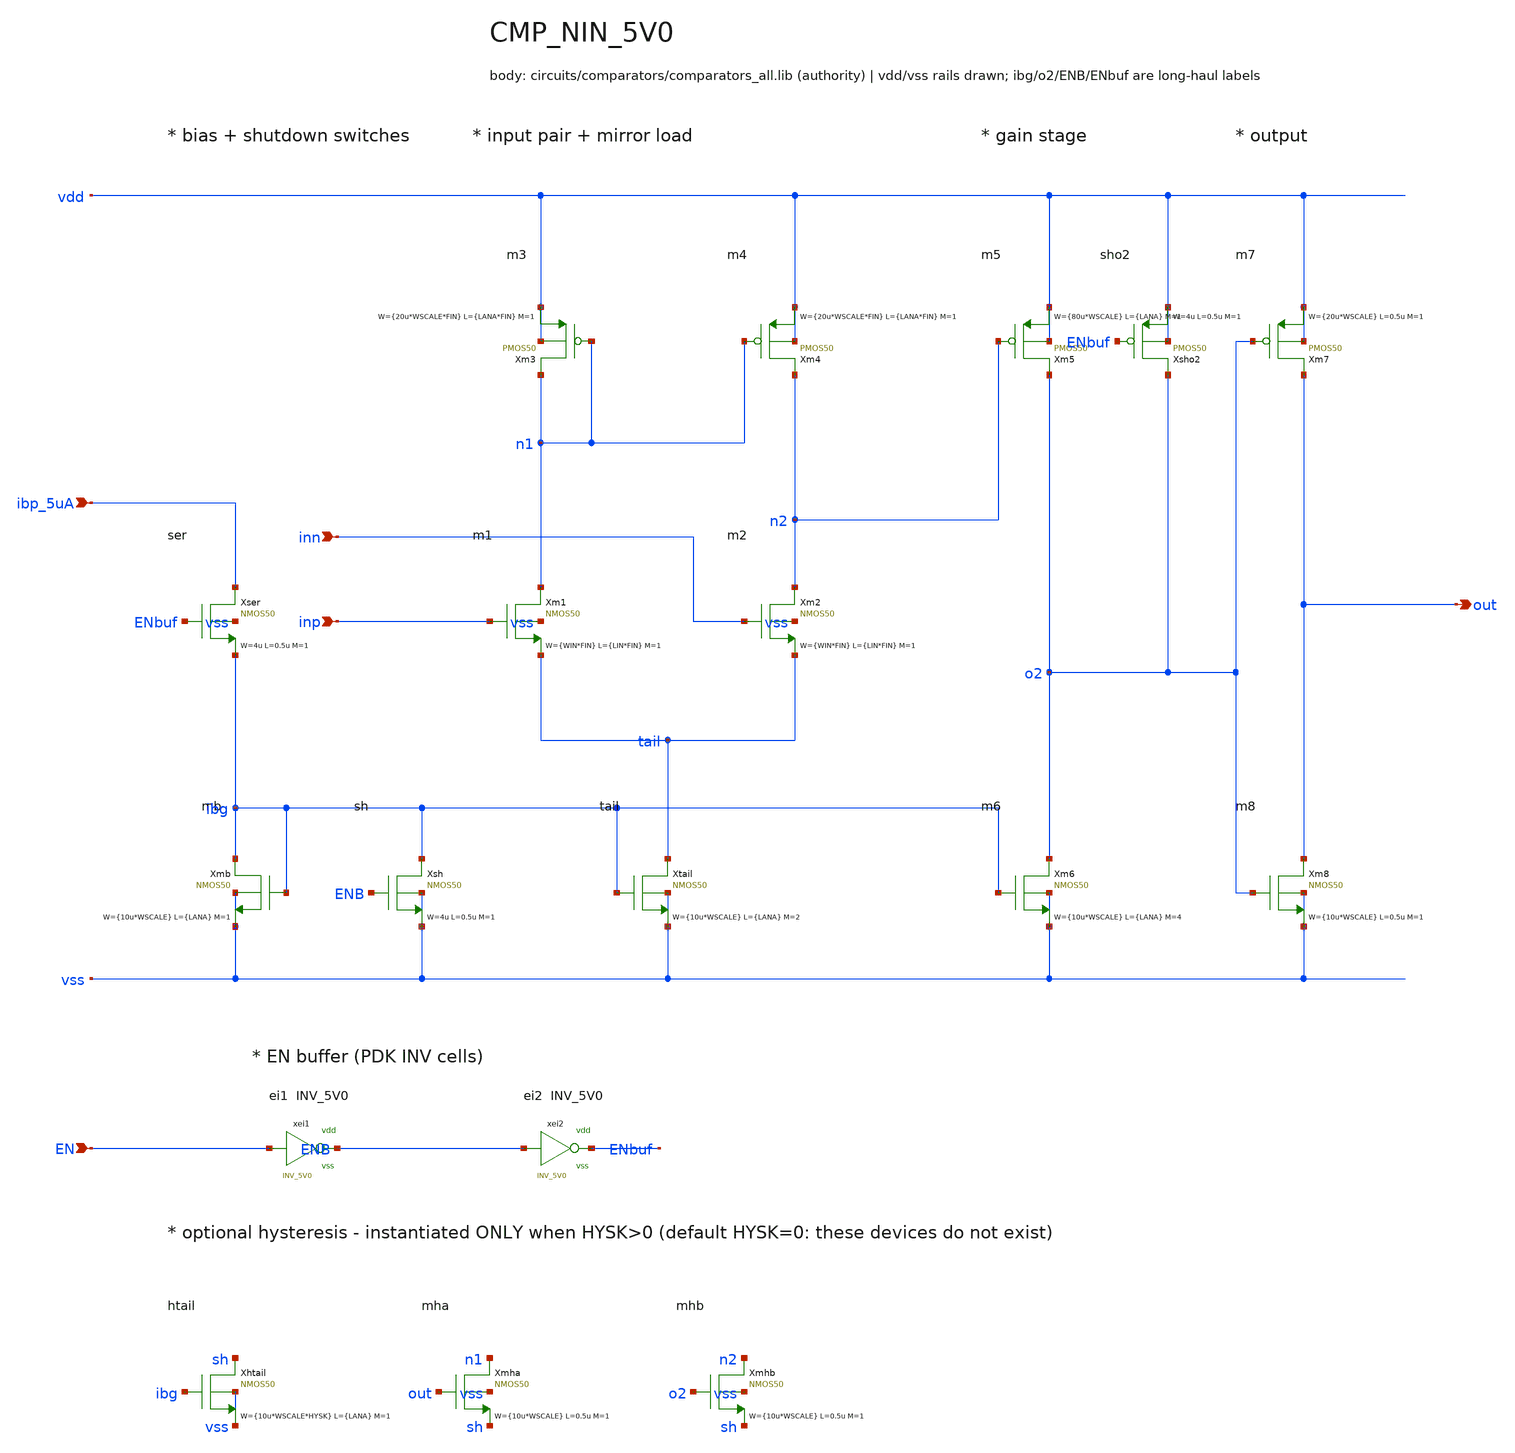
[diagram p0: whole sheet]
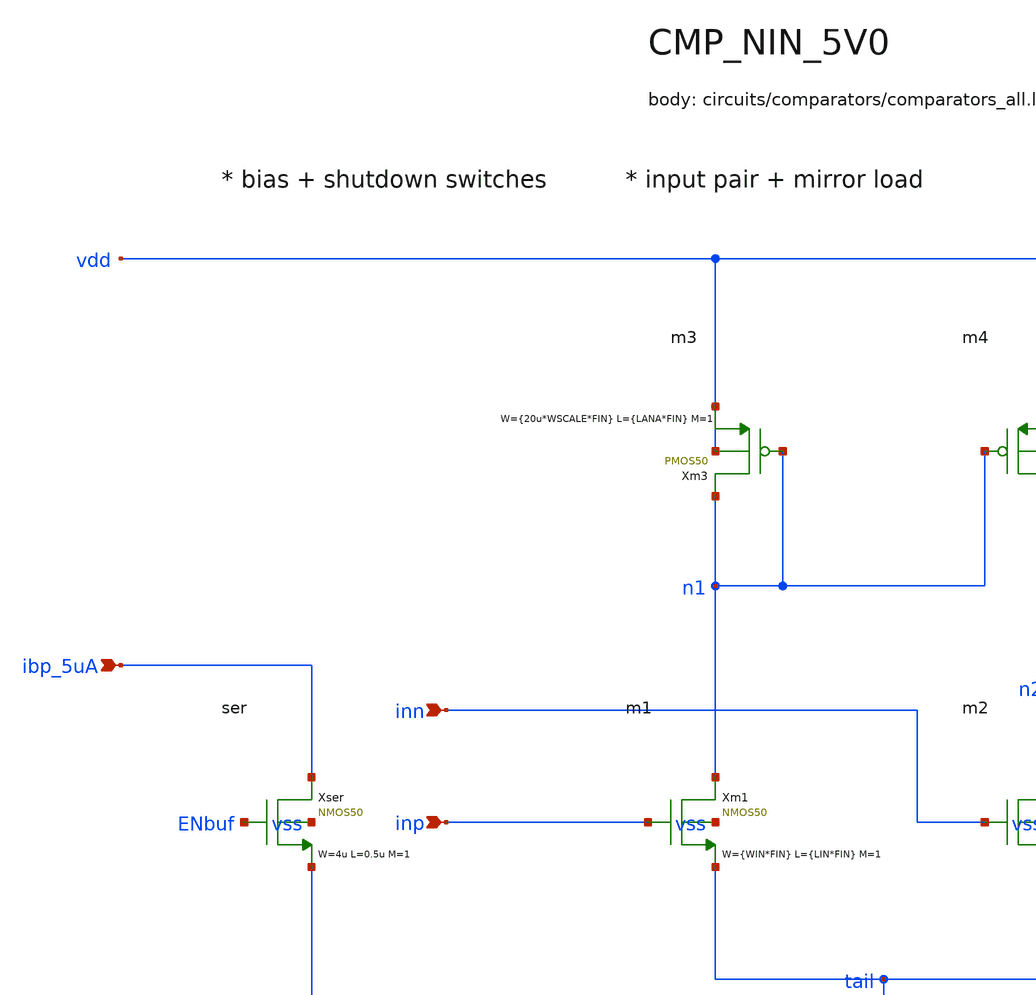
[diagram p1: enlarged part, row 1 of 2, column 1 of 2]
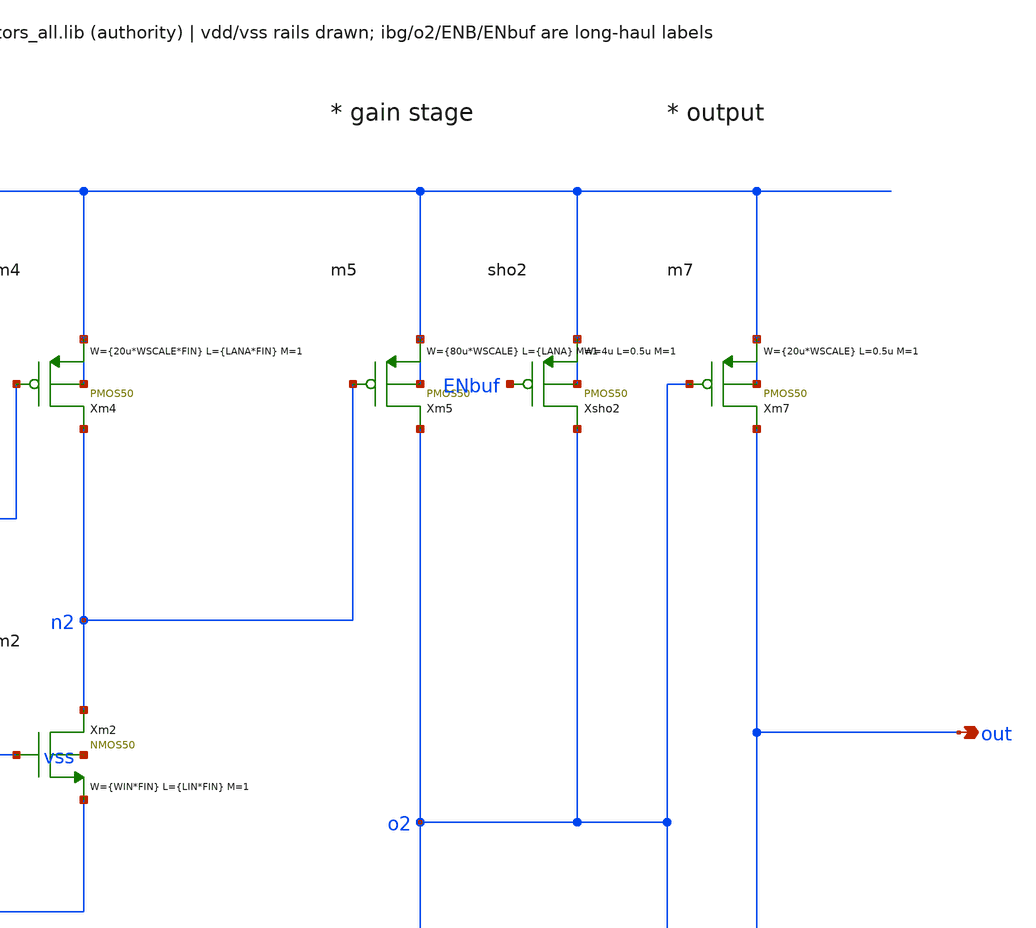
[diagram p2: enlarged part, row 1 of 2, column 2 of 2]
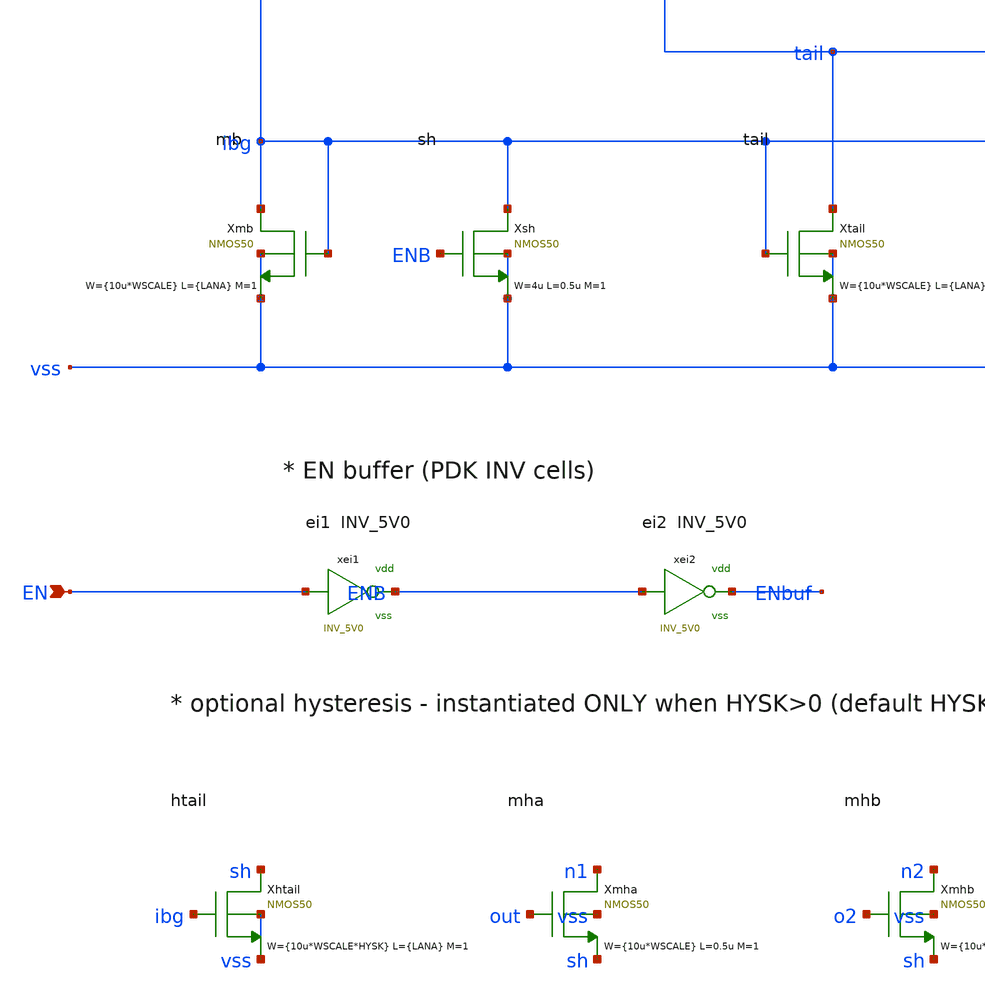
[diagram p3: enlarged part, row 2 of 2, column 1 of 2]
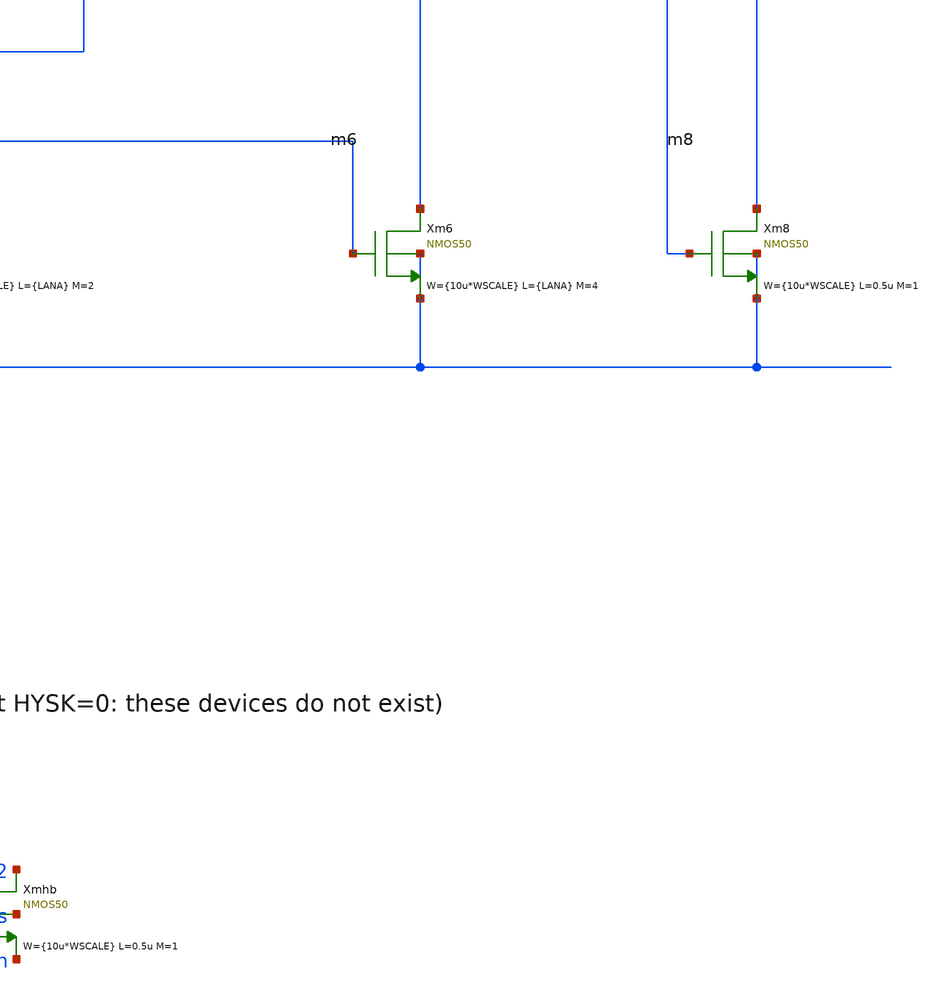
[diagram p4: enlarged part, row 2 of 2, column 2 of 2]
** sch_path: xschem/comparators/CMP_NIN_5V0.sch
**.subckt CMP_NIN_5V0 ibp_5uA out inp inn EN
*.ipin ibp_5uA
*.opin out
*.ipin inp
*.ipin inn
*.ipin EN
Xmb ibg ibg vss vss NMOS50 W={10u*WSCALE} L={LANA} M=1 MM_SIGMA=0
Xtail tail ibg vss vss NMOS50 W={10u*WSCALE} L={LANA} M=2 MM_SIGMA=0
Xm1 n1 inp tail vss NMOS50 W={WIN*FIN} L={LIN*FIN} M=1 MM_SIGMA=0
Xm2 n2 inn tail vss NMOS50 W={WIN*FIN} L={LIN*FIN} M=1 MM_SIGMA=0
Xm3 n1 n1 vdd vdd PMOS50 W={20u*WSCALE*FIN} L={LANA*FIN} M=1 MM_SIGMA=0
Xm4 n2 n1 vdd vdd PMOS50 W={20u*WSCALE*FIN} L={LANA*FIN} M=1 MM_SIGMA=0
Xm5 o2 n2 vdd vdd PMOS50 W={80u*WSCALE} L={LANA} M=1 MM_SIGMA=0
Xm6 o2 ibg vss vss NMOS50 W={10u*WSCALE} L={LANA} M=4 MM_SIGMA=0
Xm7 out o2 vdd vdd PMOS50 W={20u*WSCALE} L=0.5u M=1 MM_SIGMA=0
Xm8 out o2 vss vss NMOS50 W={10u*WSCALE} L=0.5u M=1 MM_SIGMA=0
xei1 EN ENB vdd vss INV_5V0
xei2 ENB ENbuf vdd vss INV_5V0
Xsh ibg ENB vss vss NMOS50 W=4u L=0.5u M=1 MM_SIGMA=0
Xsho2 o2 ENbuf vdd vdd PMOS50 W=4u L=0.5u M=1 MM_SIGMA=0
Xser ibp_5uA ENbuf ibg vss NMOS50 W=4u L=0.5u M=1 MM_SIGMA=0
Xhtail sh ibg vss vss NMOS50 W={10u*WSCALE*HYSK} L={LANA} M=1 MM_SIGMA=0
Xmha n1 out sh vss NMOS50 W={10u*WSCALE} L=0.5u M=1 MM_SIGMA=0
Xmhb n2 o2 sh vss NMOS50 W={10u*WSCALE} L=0.5u M=1 MM_SIGMA=0
**.ends

* expanding   symbol:  logic/INV_5V0.sym # of pins=2
** sym_path: xschem/logic/INV_5V0.sym
* INV_5V0 body is defined in circuits/async_logic_design/cells.lib
.end
